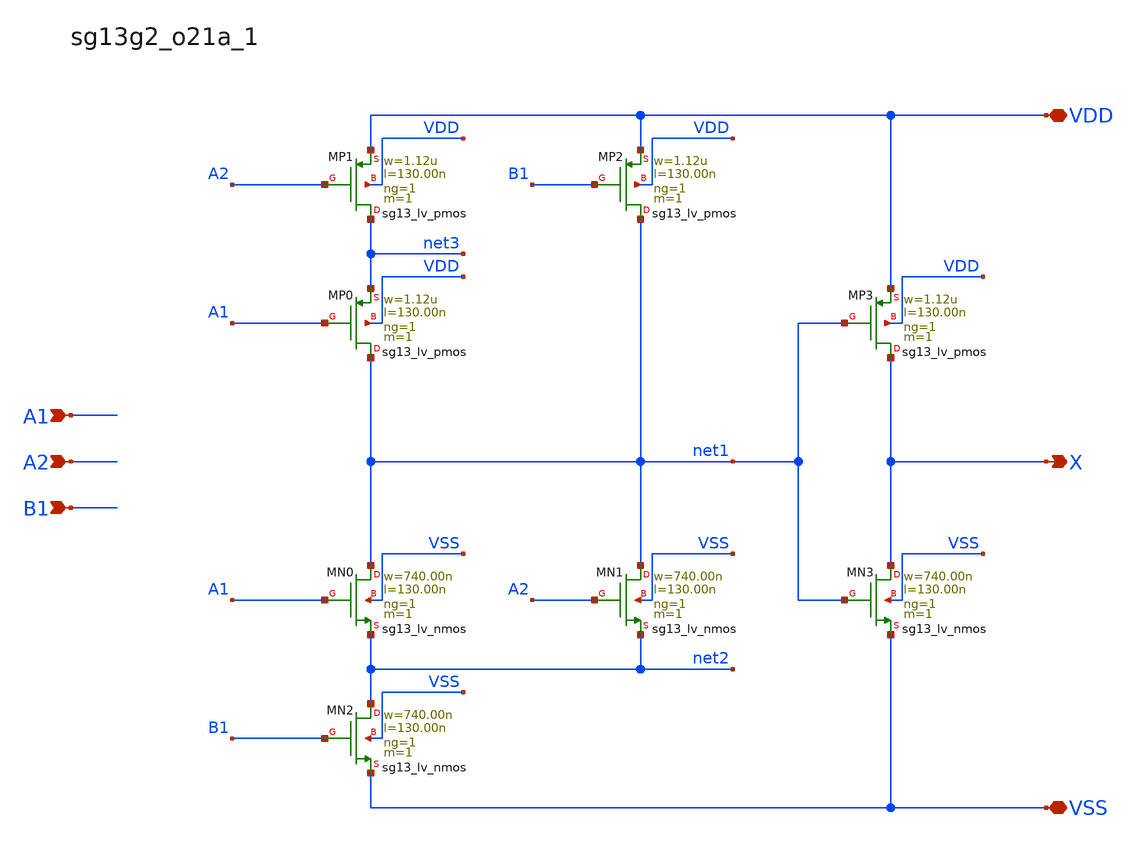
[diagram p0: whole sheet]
** sch_path: outputs/sg13g2_cells/cells/sg13g2_o21a_1/sg13g2_o21a_1.sch
**.subckt sg13g2_o21a_1 X A1 A2 B1 VDD VSS
*.opin X
*.ipin A1
*.ipin A2
*.ipin B1
*.iopin VDD
*.iopin VSS
XMN0 net1 A1 net2 VSS sg13_lv_nmos w=740.00n l=130.00n ng=1 m=1 mm_ok=1
XMN1 net1 A2 net2 VSS sg13_lv_nmos w=740.00n l=130.00n ng=1 m=1 mm_ok=1
XMN2 net2 B1 VSS VSS sg13_lv_nmos w=740.00n l=130.00n ng=1 m=1 mm_ok=1
XMP0 net1 A1 net3 VDD sg13_lv_pmos w=1.12u l=130.00n ng=1 m=1 mm_ok=1
XMP1 net3 A2 VDD VDD sg13_lv_pmos w=1.12u l=130.00n ng=1 m=1 mm_ok=1
XMP2 net1 B1 VDD VDD sg13_lv_pmos w=1.12u l=130.00n ng=1 m=1 mm_ok=1
XMN3 X net1 VSS VSS sg13_lv_nmos w=740.00n l=130.00n ng=1 m=1 mm_ok=1
XMP3 X net1 VDD VDD sg13_lv_pmos w=1.12u l=130.00n ng=1 m=1 mm_ok=1
**.ends
.end
